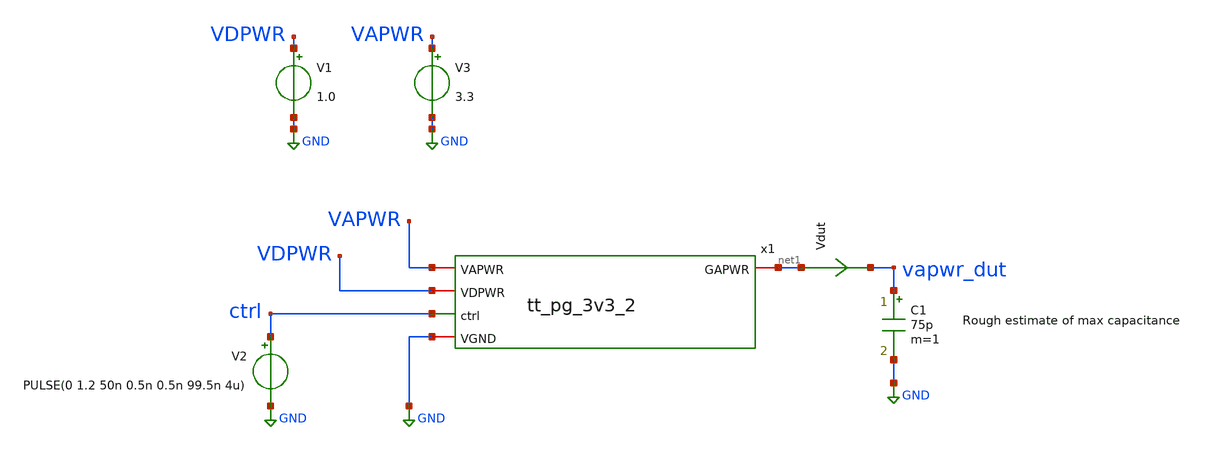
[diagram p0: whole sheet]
** sch_path: pg/ihp-sg13cmos5l/tt_pg_3v3_2/xschem/tb_switch.sch
**.subckt tb_switch
V1 VDPWR GND 1.0
.save i(v1)
C1 vapwr_dut GND 75p m=1
V2 ctrl GND PULSE(0 1.2 50n 0.5n 0.5n 99.5n 4u)
Vdut net1 vapwr_dut 0
.save i(vdut)
x1 GND VDPWR VAPWR net1 ctrl tt_pg_3v3_2
V3 VAPWR GND 3.3
.save i(v3)
**** begin user architecture code


.param mc_mm_switch=0
.control
save all
tran 50p 5u
plot vapwr_dut
plot vapwr_dut ctrl+5 x1.H_ctrl_n+10 x1.H_ctrl_p+10 xlimit 50n 60n
*quit 0
.endc
.end




.lib cornerMOSlv.lib mos_tt
.lib cornerMOShv.lib mos_tt
.lib cornerCAP.lib cap_typ


**** end user architecture code
**.ends
.GLOBAL GND
.end
